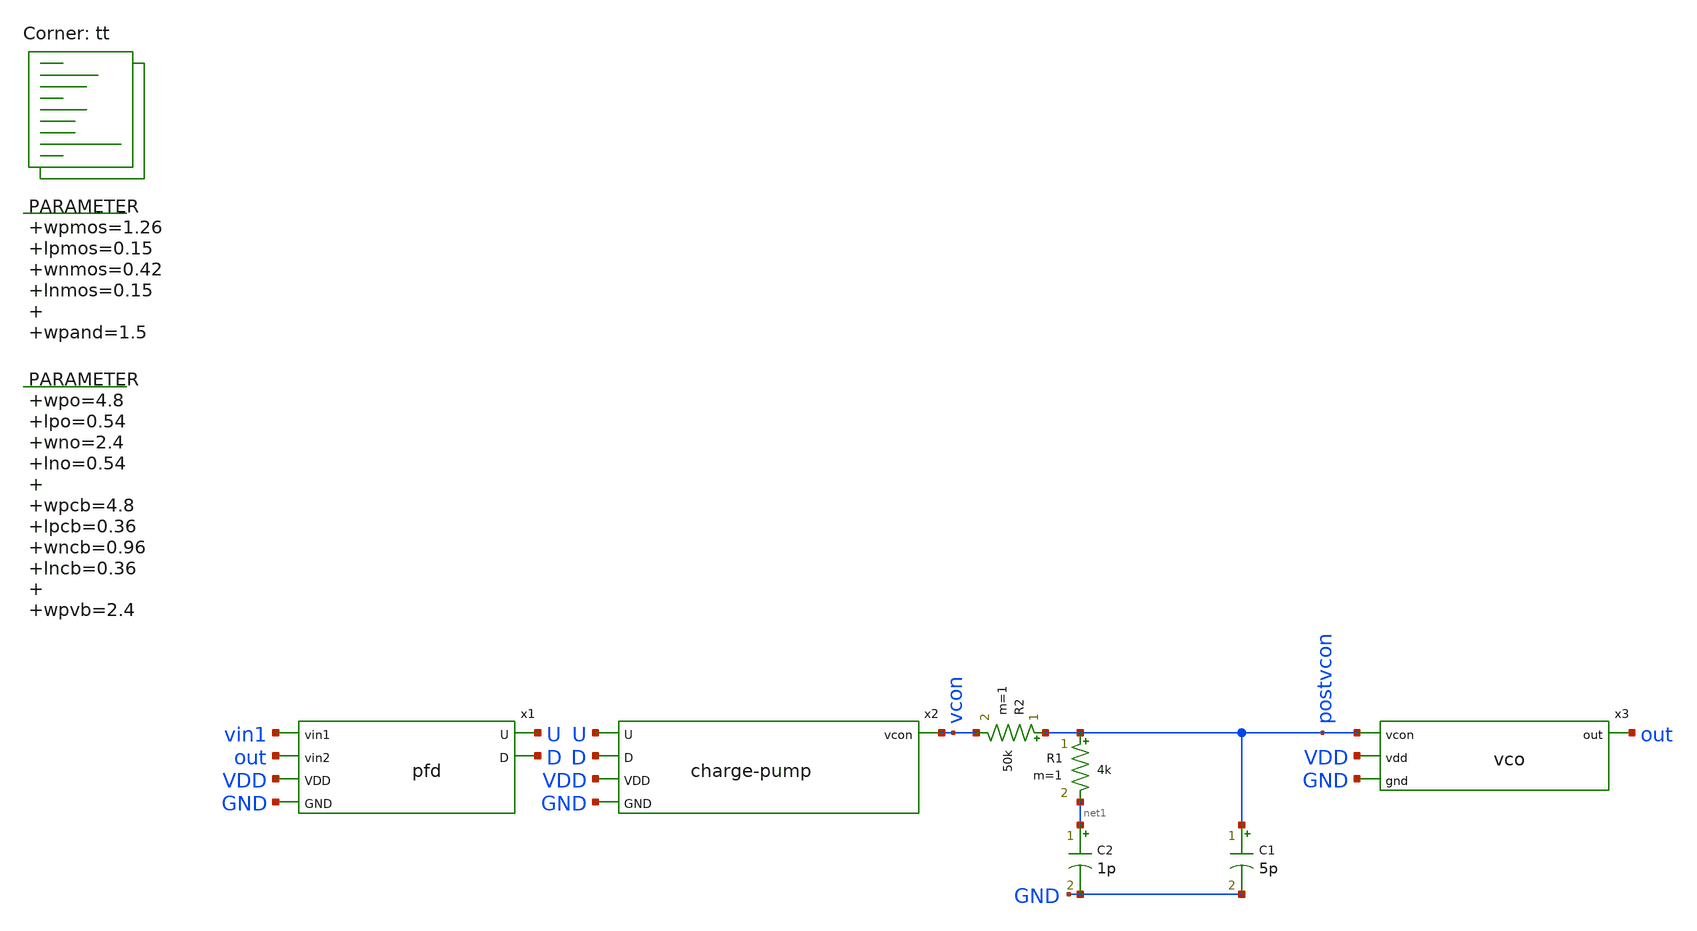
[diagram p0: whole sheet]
** sch_path: xschem/pll-tb.sch
**.subckt pll-tb
.param wpmos=1.26 lpmos=0.15 wnmos=0.42 lnmos=0.15 wpand=1.5

x2 U D vcon VDD GND charge-pump
x1 vin1 out U D VDD GND pfd
C2 net1 GND 1p m=1
R1 postvcon net1 4k m=1
R2 postvcon vcon 50k m=1
C1 postvcon GND 5p m=1
x3 postvcon out VDD GND vco
.param wpo=4.8 lpo=0.54 wno=2.4 lno=0.54 wpcb=4.8 lpcb=0.36 wncb=0.96 lncb=0.36 wpvb=2.4 lpvb=0.36
+ wnvc=96 lnvc=0.9 wpbuff=4.8 lpbuff=0.18 wnbuff=1.2 lnbuff=0.18 lres=3.5

**** begin user architecture code
 .lib $::SKYWATER_MODELS/sky130.lib.spice tt
.include $::SKYWATER_STDCELLS/sky130_fd_sc_hd.spice
.param mc_mm_switch = 0
.param mc_pr_switch = 0




  .param max_freq=100e6 period={1/max_freq} time_high={period/2}
  .param delay_vin1={time_high} delay_vin2={time_high*1.5}

  .option wnflag=1
  .option safecurrents

  *Vvdd  VDDA  VSS dc 1.8
  Vvdd1 VDD   GND dc 1.8
  Vin1 vin1 GND pulse(0 1.8 {delay_vin1} 1p 1p {time_high} {period})
  *Vin2 vin2 gnd pulse(0 1.8 {delay_vin2} 1p 1p {time_high} {period})

  .control
     reset
     save all
     tran 0.01n 1u
     write pll-tb.raw
     *set appendwrite

     *1=0 1.5=90 2=180 3=360
     *let phase=1

     *while phase <= 2
      *alter @vin2[PULSE] [ 0 1.8 {delay_vin2*$&phase} 1p 1p {time_high} {period}) ]
      *reset
      *save all
      *tran 0.01n 300n
      *write pll-tb.raw
      *let phase = phase + 0.25
     *end
    quit 0
  .endc



**** end user architecture code
**.ends

* expanding   symbol:  charge-pump.sym # of pins=5
** sym_path: xschem/charge-pump.sym
** sch_path: xschem/charge-pump.sch
.subckt charge-pump U D vcon VDD GND
*.ipin U
*.ipin D
*.opin vcon
*.ipin VDD
*.ipin GND
XM1 vcon Ub VDD VDD sky130_fd_pr__pfet_01v8 L=0.36 W=4.8 nf=1 ad='int((nf+1)/2) * W/nf * 0.29' as='int((nf+2)/2) * W/nf * 0.29'
+ pd='2*int((nf+1)/2) * (W/nf + 0.29)' ps='2*int((nf+2)/2) * (W/nf + 0.29)' nrd='0.29 / W' nrs='0.29 / W'
+ sa=0 sb=0 sd=0 mult=1 m=1
XM2 vcon D GND GND sky130_fd_pr__nfet_01v8 L=0.36 W=0.96 nf=1 ad='int((nf+1)/2) * W/nf * 0.29' as='int((nf+2)/2) * W/nf * 0.29'
+ pd='2*int((nf+1)/2) * (W/nf + 0.29)' ps='2*int((nf+2)/2) * (W/nf + 0.29)' nrd='0.29 / W' nrs='0.29 / W'
+ sa=0 sb=0 sd=0 mult=1 m=1
XM3 Ub U VDD VDD sky130_fd_pr__pfet_01v8 L=0.18 W=4.8 nf=1 ad='int((nf+1)/2) * W/nf * 0.29' as='int((nf+2)/2) * W/nf * 0.29'
+ pd='2*int((nf+1)/2) * (W/nf + 0.29)' ps='2*int((nf+2)/2) * (W/nf + 0.29)' nrd='0.29 / W' nrs='0.29 / W'
+ sa=0 sb=0 sd=0 mult=1 m=1
XM4 Ub U GND GND sky130_fd_pr__nfet_01v8 L=0.18 W=1.2 nf=1 ad='int((nf+1)/2) * W/nf * 0.29' as='int((nf+2)/2) * W/nf * 0.29'
+ pd='2*int((nf+1)/2) * (W/nf + 0.29)' ps='2*int((nf+2)/2) * (W/nf + 0.29)' nrd='0.29 / W' nrs='0.29 / W'
+ sa=0 sb=0 sd=0 mult=1 m=1
.ends


* expanding   symbol:  pfd.sym # of pins=6
** sym_path: xschem/pfd.sym
** sch_path: xschem/pfd.sch
.subckt pfd vin1 vin2 U D VDD GND
*.ipin vin1
*.ipin vin2
*.opin U
*.opin D
*.ipin VDD
*.ipin GND
.param wpmos=1.26 lpmos=0.15 wnmos=0.42 lnmos=0.15 wpand=1.5

XM1 net4 rst GND GND sky130_fd_pr__nfet_01v8 L=lnmos W=wnmos nf=1 ad='int((nf+1)/2) * W/nf * 0.29' as='int((nf+2)/2) * W/nf * 0.29'
+ pd='2*int((nf+1)/2) * (W/nf + 0.29)' ps='2*int((nf+2)/2) * (W/nf + 0.29)' nrd='0.29 / W' nrs='0.29 / W'
+ sa=0 sb=0 sd=0 mult=1 m=1
XM2 net3 vin1 VDD VDD sky130_fd_pr__pfet_01v8 L=lpmos W=wpmos nf=1 ad='int((nf+1)/2) * W/nf * 0.29' as='int((nf+2)/2) * W/nf * 0.29'
+ pd='2*int((nf+1)/2) * (W/nf + 0.29)' ps='2*int((nf+2)/2) * (W/nf + 0.29)' nrd='0.29 / W' nrs='0.29 / W'
+ sa=0 sb=0 sd=0 mult=1 m=1
XM3 net4 rst net3 VDD sky130_fd_pr__pfet_01v8 L=lpmos W=wpmos nf=1 ad='int((nf+1)/2) * W/nf * 0.29' as='int((nf+2)/2) * W/nf * 0.29'
+ pd='2*int((nf+1)/2) * (W/nf + 0.29)' ps='2*int((nf+2)/2) * (W/nf + 0.29)' nrd='0.29 / W' nrs='0.29 / W'
+ sa=0 sb=0 sd=0 mult=1 m=1
XM4 net1 net4 VDD VDD sky130_fd_pr__pfet_01v8 L=lpmos W=wpmos nf=1 ad='int((nf+1)/2) * W/nf * 0.29' as='int((nf+2)/2) * W/nf * 0.29'
+ pd='2*int((nf+1)/2) * (W/nf + 0.29)' ps='2*int((nf+2)/2) * (W/nf + 0.29)' nrd='0.29 / W' nrs='0.29 / W'
+ sa=0 sb=0 sd=0 mult=1 m=1
XM5 preU net1 VDD VDD sky130_fd_pr__pfet_01v8 L=lpmos W=wpmos nf=1 ad='int((nf+1)/2) * W/nf * 0.29' as='int((nf+2)/2) * W/nf * 0.29'
+ pd='2*int((nf+1)/2) * (W/nf + 0.29)' ps='2*int((nf+2)/2) * (W/nf + 0.29)' nrd='0.29 / W' nrs='0.29 / W'
+ sa=0 sb=0 sd=0 mult=1 m=1
XM6 net1 net4 net2 GND sky130_fd_pr__nfet_01v8 L=lnmos W=wnmos nf=1 ad='int((nf+1)/2) * W/nf * 0.29'
+ as='int((nf+2)/2) * W/nf * 0.29' pd='2*int((nf+1)/2) * (W/nf + 0.29)' ps='2*int((nf+2)/2) * (W/nf + 0.29)'
+ nrd='0.29 / W' nrs='0.29 / W' sa=0 sb=0 sd=0 mult=1 m=1
XM7 preU net1 GND GND sky130_fd_pr__nfet_01v8 L=lnmos W=wnmos nf=1 ad='int((nf+1)/2) * W/nf * 0.29' as='int((nf+2)/2) * W/nf * 0.29'
+ pd='2*int((nf+1)/2) * (W/nf + 0.29)' ps='2*int((nf+2)/2) * (W/nf + 0.29)' nrd='0.29 / W' nrs='0.29 / W'
+ sa=0 sb=0 sd=0 mult=1 m=1
XM8 net2 vin1 GND GND sky130_fd_pr__nfet_01v8 L=lnmos W=wnmos nf=1 ad='int((nf+1)/2) * W/nf * 0.29' as='int((nf+2)/2) * W/nf * 0.29'
+ pd='2*int((nf+1)/2) * (W/nf + 0.29)' ps='2*int((nf+2)/2) * (W/nf + 0.29)' nrd='0.29 / W' nrs='0.29 / W'
+ sa=0 sb=0 sd=0 mult=1 m=1
XM10 net6 vin2 VDD VDD sky130_fd_pr__pfet_01v8 L=lpmos W=wpmos nf=1 ad='int((nf+1)/2) * W/nf * 0.29'
+ as='int((nf+2)/2) * W/nf * 0.29' pd='2*int((nf+1)/2) * (W/nf + 0.29)' ps='2*int((nf+2)/2) * (W/nf + 0.29)'
+ nrd='0.29 / W' nrs='0.29 / W' sa=0 sb=0 sd=0 mult=1 m=1
XM11 net5 net7 VDD VDD sky130_fd_pr__pfet_01v8 L=lpmos W=wpmos nf=1 ad='int((nf+1)/2) * W/nf * 0.29'
+ as='int((nf+2)/2) * W/nf * 0.29' pd='2*int((nf+1)/2) * (W/nf + 0.29)' ps='2*int((nf+2)/2) * (W/nf + 0.29)'
+ nrd='0.29 / W' nrs='0.29 / W' sa=0 sb=0 sd=0 mult=1 m=1
XM12 net7 rst net6 VDD sky130_fd_pr__pfet_01v8 L=lpmos W=wpmos nf=1 ad='int((nf+1)/2) * W/nf * 0.29'
+ as='int((nf+2)/2) * W/nf * 0.29' pd='2*int((nf+1)/2) * (W/nf + 0.29)' ps='2*int((nf+2)/2) * (W/nf + 0.29)'
+ nrd='0.29 / W' nrs='0.29 / W' sa=0 sb=0 sd=0 mult=1 m=1
XM13 preD net5 VDD VDD sky130_fd_pr__pfet_01v8 L=lpmos W=wpmos nf=1 ad='int((nf+1)/2) * W/nf * 0.29'
+ as='int((nf+2)/2) * W/nf * 0.29' pd='2*int((nf+1)/2) * (W/nf + 0.29)' ps='2*int((nf+2)/2) * (W/nf + 0.29)'
+ nrd='0.29 / W' nrs='0.29 / W' sa=0 sb=0 sd=0 mult=1 m=1
XM14 net7 rst GND GND sky130_fd_pr__nfet_01v8 L=lnmos W=wnmos nf=1 ad='int((nf+1)/2) * W/nf * 0.29' as='int((nf+2)/2) * W/nf * 0.29'
+ pd='2*int((nf+1)/2) * (W/nf + 0.29)' ps='2*int((nf+2)/2) * (W/nf + 0.29)' nrd='0.29 / W' nrs='0.29 / W'
+ sa=0 sb=0 sd=0 mult=1 m=1
XM15 net5 net7 net8 GND sky130_fd_pr__nfet_01v8 L=lnmos W=wnmos nf=1 ad='int((nf+1)/2) * W/nf * 0.29'
+ as='int((nf+2)/2) * W/nf * 0.29' pd='2*int((nf+1)/2) * (W/nf + 0.29)' ps='2*int((nf+2)/2) * (W/nf + 0.29)'
+ nrd='0.29 / W' nrs='0.29 / W' sa=0 sb=0 sd=0 mult=1 m=1
XM16 preD net5 GND GND sky130_fd_pr__nfet_01v8 L=lnmos W=wnmos nf=1 ad='int((nf+1)/2) * W/nf * 0.29'
+ as='int((nf+2)/2) * W/nf * 0.29' pd='2*int((nf+1)/2) * (W/nf + 0.29)' ps='2*int((nf+2)/2) * (W/nf + 0.29)'
+ nrd='0.29 / W' nrs='0.29 / W' sa=0 sb=0 sd=0 mult=1 m=1
XM18 net8 vin2 GND GND sky130_fd_pr__nfet_01v8 L=lnmos W=wnmos nf=1 ad='int((nf+1)/2) * W/nf * 0.29'
+ as='int((nf+2)/2) * W/nf * 0.29' pd='2*int((nf+1)/2) * (W/nf + 0.29)' ps='2*int((nf+2)/2) * (W/nf + 0.29)'
+ nrd='0.29 / W' nrs='0.29 / W' sa=0 sb=0 sd=0 mult=1 m=1
x1 preU GND GND VDD VDD U sky130_fd_sc_hd__buf_8
x2 preD GND GND VDD VDD D sky130_fd_sc_hd__buf_8
x3 prerst GND GND VDD VDD rst sky130_fd_sc_hd__buf_1
x4 U D GND GND VDD VDD prerst sky130_fd_sc_hd__and2_1
.ends


* expanding   symbol:  vco.sym # of pins=4
** sym_path: xschem/vco.sym
** sch_path: xschem/vco.sch
.subckt vco vcon out vdd gnd
*.ipin vcon
*.opin out
*.ipin vdd
*.ipin gnd
.param wpo=4.8 lpo=0.54 wno=2.4 lno=0.54 wpcb=4.8 lpcb=0.36 wncb=0.96 lncb=0.36 wpvb=6 lpvb=0.9
+ wnvc=96 lnvc=0.9 wpbuff=4.8 lpbuff=0.18 wnbuff=1.2 lnbuff=0.18 lres=3.5

XM1 vnbias vnbias gnd gnd sky130_fd_pr__nfet_01v8 L=lncb W=wncb nf=1 ad='int((nf+1)/2) * W/nf * 0.29'
+ as='int((nf+2)/2) * W/nf * 0.29' pd='2*int((nf+1)/2) * (W/nf + 0.29)' ps='2*int((nf+2)/2) * (W/nf + 0.29)'
+ nrd='0.29 / W' nrs='0.29 / W' sa=0 sb=0 sd=0 mult=1 m=1
XM2 vpbias vpbias vdd vdd sky130_fd_pr__pfet_01v8 L=lpvb W=wpvb nf=1 ad='int((nf+1)/2) * W/nf * 0.29'
+ as='int((nf+2)/2) * W/nf * 0.29' pd='2*int((nf+1)/2) * (W/nf + 0.29)' ps='2*int((nf+2)/2) * (W/nf + 0.29)'
+ nrd='0.29 / W' nrs='0.29 / W' sa=0 sb=0 sd=0 mult=1 m=1
XM4 vnbias vpbias vdd vdd sky130_fd_pr__pfet_01v8 L=lpcb W=wpcb nf=1 ad='int((nf+1)/2) * W/nf * 0.29'
+ as='int((nf+2)/2) * W/nf * 0.29' pd='2*int((nf+1)/2) * (W/nf + 0.29)' ps='2*int((nf+2)/2) * (W/nf + 0.29)'
+ nrd='0.29 / W' nrs='0.29 / W' sa=0 sb=0 sd=0 mult=1 m=1
XM5 net8 net9 net1 gnd sky130_fd_pr__nfet_01v8 L=lno W=wno nf=1 ad='int((nf+1)/2) * W/nf * 0.29' as='int((nf+2)/2) * W/nf * 0.29'
+ pd='2*int((nf+1)/2) * (W/nf + 0.29)' ps='2*int((nf+2)/2) * (W/nf + 0.29)' nrd='0.29 / W' nrs='0.29 / W'
+ sa=0 sb=0 sd=0 mult=1 m=1
XM6 net8 net9 net12 vdd sky130_fd_pr__pfet_01v8 L=lpo W=wpo nf=1 ad='int((nf+1)/2) * W/nf * 0.29' as='int((nf+2)/2) * W/nf * 0.29'
+ pd='2*int((nf+1)/2) * (W/nf + 0.29)' ps='2*int((nf+2)/2) * (W/nf + 0.29)' nrd='0.29 / W' nrs='0.29 / W'
+ sa=0 sb=0 sd=0 mult=1 m=1
XM7 net7 net8 net2 gnd sky130_fd_pr__nfet_01v8 L=lno W=wno nf=1 ad='int((nf+1)/2) * W/nf * 0.29' as='int((nf+2)/2) * W/nf * 0.29'
+ pd='2*int((nf+1)/2) * (W/nf + 0.29)' ps='2*int((nf+2)/2) * (W/nf + 0.29)' nrd='0.29 / W' nrs='0.29 / W'
+ sa=0 sb=0 sd=0 mult=1 m=1
XM8 net7 net8 net13 vdd sky130_fd_pr__pfet_01v8 L=lpo W=wpo nf=1 ad='int((nf+1)/2) * W/nf * 0.29' as='int((nf+2)/2) * W/nf * 0.29'
+ pd='2*int((nf+1)/2) * (W/nf + 0.29)' ps='2*int((nf+2)/2) * (W/nf + 0.29)' nrd='0.29 / W' nrs='0.29 / W'
+ sa=0 sb=0 sd=0 mult=1 m=1
XM9 net6 net7 net3 gnd sky130_fd_pr__nfet_01v8 L=lno W=wno nf=1 ad='int((nf+1)/2) * W/nf * 0.29' as='int((nf+2)/2) * W/nf * 0.29'
+ pd='2*int((nf+1)/2) * (W/nf + 0.29)' ps='2*int((nf+2)/2) * (W/nf + 0.29)' nrd='0.29 / W' nrs='0.29 / W'
+ sa=0 sb=0 sd=0 mult=1 m=1
XM10 net6 net7 net14 vdd sky130_fd_pr__pfet_01v8 L=lpo W=wpo nf=1 ad='int((nf+1)/2) * W/nf * 0.29' as='int((nf+2)/2) * W/nf * 0.29'
+ pd='2*int((nf+1)/2) * (W/nf + 0.29)' ps='2*int((nf+2)/2) * (W/nf + 0.29)' nrd='0.29 / W' nrs='0.29 / W'
+ sa=0 sb=0 sd=0 mult=1 m=1
XM11 net10 net6 net5 gnd sky130_fd_pr__nfet_01v8 L=lno W=wno nf=1 ad='int((nf+1)/2) * W/nf * 0.29' as='int((nf+2)/2) * W/nf * 0.29'
+ pd='2*int((nf+1)/2) * (W/nf + 0.29)' ps='2*int((nf+2)/2) * (W/nf + 0.29)' nrd='0.29 / W' nrs='0.29 / W'
+ sa=0 sb=0 sd=0 mult=1 m=1
XM12 net10 net6 net15 vdd sky130_fd_pr__pfet_01v8 L=lpo W=wpo nf=1 ad='int((nf+1)/2) * W/nf * 0.29' as='int((nf+2)/2) * W/nf * 0.29'
+ pd='2*int((nf+1)/2) * (W/nf + 0.29)' ps='2*int((nf+2)/2) * (W/nf + 0.29)' nrd='0.29 / W' nrs='0.29 / W'
+ sa=0 sb=0 sd=0 mult=1 m=1
XM13 net9 net10 net4 gnd sky130_fd_pr__nfet_01v8 L=lno W=wno nf=1 ad='int((nf+1)/2) * W/nf * 0.29' as='int((nf+2)/2) * W/nf * 0.29'
+ pd='2*int((nf+1)/2) * (W/nf + 0.29)' ps='2*int((nf+2)/2) * (W/nf + 0.29)' nrd='0.29 / W' nrs='0.29 / W'
+ sa=0 sb=0 sd=0 mult=1 m=1
XM14 net9 net10 net16 vdd sky130_fd_pr__pfet_01v8 L=lpo W=wpo nf=1 ad='int((nf+1)/2) * W/nf * 0.29' as='int((nf+2)/2) * W/nf * 0.29'
+ pd='2*int((nf+1)/2) * (W/nf + 0.29)' ps='2*int((nf+2)/2) * (W/nf + 0.29)' nrd='0.29 / W' nrs='0.29 / W'
+ sa=0 sb=0 sd=0 mult=1 m=1
XM16 net12 vpbias vdd vdd sky130_fd_pr__pfet_01v8 L=lpcb W=wpcb nf=1 ad='int((nf+1)/2) * W/nf * 0.29'
+ as='int((nf+2)/2) * W/nf * 0.29' pd='2*int((nf+1)/2) * (W/nf + 0.29)' ps='2*int((nf+2)/2) * (W/nf + 0.29)'
+ nrd='0.29 / W' nrs='0.29 / W' sa=0 sb=0 sd=0 mult=1 m=1
XM18 net13 vpbias vdd vdd sky130_fd_pr__pfet_01v8 L=lpcb W=wpcb nf=1 ad='int((nf+1)/2) * W/nf * 0.29'
+ as='int((nf+2)/2) * W/nf * 0.29' pd='2*int((nf+1)/2) * (W/nf + 0.29)' ps='2*int((nf+2)/2) * (W/nf + 0.29)'
+ nrd='0.29 / W' nrs='0.29 / W' sa=0 sb=0 sd=0 mult=1 m=1
XM20 net14 vpbias vdd vdd sky130_fd_pr__pfet_01v8 L=lpcb W=wpcb nf=1 ad='int((nf+1)/2) * W/nf * 0.29'
+ as='int((nf+2)/2) * W/nf * 0.29' pd='2*int((nf+1)/2) * (W/nf + 0.29)' ps='2*int((nf+2)/2) * (W/nf + 0.29)'
+ nrd='0.29 / W' nrs='0.29 / W' sa=0 sb=0 sd=0 mult=1 m=1
XM22 net15 vpbias vdd vdd sky130_fd_pr__pfet_01v8 L=lpcb W=wpcb nf=1 ad='int((nf+1)/2) * W/nf * 0.29'
+ as='int((nf+2)/2) * W/nf * 0.29' pd='2*int((nf+1)/2) * (W/nf + 0.29)' ps='2*int((nf+2)/2) * (W/nf + 0.29)'
+ nrd='0.29 / W' nrs='0.29 / W' sa=0 sb=0 sd=0 mult=1 m=1
XM24 net16 vpbias vdd vdd sky130_fd_pr__pfet_01v8 L=lpcb W=wpcb nf=1 ad='int((nf+1)/2) * W/nf * 0.29'
+ as='int((nf+2)/2) * W/nf * 0.29' pd='2*int((nf+1)/2) * (W/nf + 0.29)' ps='2*int((nf+2)/2) * (W/nf + 0.29)'
+ nrd='0.29 / W' nrs='0.29 / W' sa=0 sb=0 sd=0 mult=1 m=1
XM25 net11 net9 gnd gnd sky130_fd_pr__nfet_01v8 L=lnbuff W=wnbuff nf=1 ad='int((nf+1)/2) * W/nf * 0.29'
+ as='int((nf+2)/2) * W/nf * 0.29' pd='2*int((nf+1)/2) * (W/nf + 0.29)' ps='2*int((nf+2)/2) * (W/nf + 0.29)'
+ nrd='0.29 / W' nrs='0.29 / W' sa=0 sb=0 sd=0 mult=1 m=1
XM26 net11 net9 vdd vdd sky130_fd_pr__pfet_01v8 L=lpbuff W=wpbuff nf=1 ad='int((nf+1)/2) * W/nf * 0.29'
+ as='int((nf+2)/2) * W/nf * 0.29' pd='2*int((nf+1)/2) * (W/nf + 0.29)' ps='2*int((nf+2)/2) * (W/nf + 0.29)'
+ nrd='0.29 / W' nrs='0.29 / W' sa=0 sb=0 sd=0 mult=1 m=1
XM27 out net11 gnd gnd sky130_fd_pr__nfet_01v8 L=lnbuff W=wnbuff nf=1 ad='int((nf+1)/2) * W/nf * 0.29'
+ as='int((nf+2)/2) * W/nf * 0.29' pd='2*int((nf+1)/2) * (W/nf + 0.29)' ps='2*int((nf+2)/2) * (W/nf + 0.29)'
+ nrd='0.29 / W' nrs='0.29 / W' sa=0 sb=0 sd=0 mult=1 m=1
XM28 out net11 vdd vdd sky130_fd_pr__pfet_01v8 L=lpbuff W=wpbuff nf=1 ad='int((nf+1)/2) * W/nf * 0.29'
+ as='int((nf+2)/2) * W/nf * 0.29' pd='2*int((nf+1)/2) * (W/nf + 0.29)' ps='2*int((nf+2)/2) * (W/nf + 0.29)'
+ nrd='0.29 / W' nrs='0.29 / W' sa=0 sb=0 sd=0 mult=1 m=1
XM15 net1 vnbias gnd gnd sky130_fd_pr__nfet_01v8 L=lncb W=wncb nf=1 ad='int((nf+1)/2) * W/nf * 0.29'
+ as='int((nf+2)/2) * W/nf * 0.29' pd='2*int((nf+1)/2) * (W/nf + 0.29)' ps='2*int((nf+2)/2) * (W/nf + 0.29)'
+ nrd='0.29 / W' nrs='0.29 / W' sa=0 sb=0 sd=0 mult=1 m=1
XM17 net2 vnbias gnd gnd sky130_fd_pr__nfet_01v8 L=lncb W=wncb nf=1 ad='int((nf+1)/2) * W/nf * 0.29'
+ as='int((nf+2)/2) * W/nf * 0.29' pd='2*int((nf+1)/2) * (W/nf + 0.29)' ps='2*int((nf+2)/2) * (W/nf + 0.29)'
+ nrd='0.29 / W' nrs='0.29 / W' sa=0 sb=0 sd=0 mult=1 m=1
XM19 net3 vnbias gnd gnd sky130_fd_pr__nfet_01v8 L=lncb W=wncb nf=1 ad='int((nf+1)/2) * W/nf * 0.29'
+ as='int((nf+2)/2) * W/nf * 0.29' pd='2*int((nf+1)/2) * (W/nf + 0.29)' ps='2*int((nf+2)/2) * (W/nf + 0.29)'
+ nrd='0.29 / W' nrs='0.29 / W' sa=0 sb=0 sd=0 mult=1 m=1
XM21 net5 vnbias gnd gnd sky130_fd_pr__nfet_01v8 L=lncb W=wncb nf=1 ad='int((nf+1)/2) * W/nf * 0.29'
+ as='int((nf+2)/2) * W/nf * 0.29' pd='2*int((nf+1)/2) * (W/nf + 0.29)' ps='2*int((nf+2)/2) * (W/nf + 0.29)'
+ nrd='0.29 / W' nrs='0.29 / W' sa=0 sb=0 sd=0 mult=1 m=1
XM23 net4 vnbias gnd gnd sky130_fd_pr__nfet_01v8 L=lncb W=wncb nf=1 ad='int((nf+1)/2) * W/nf * 0.29'
+ as='int((nf+2)/2) * W/nf * 0.29' pd='2*int((nf+1)/2) * (W/nf + 0.29)' ps='2*int((nf+2)/2) * (W/nf + 0.29)'
+ nrd='0.29 / W' nrs='0.29 / W' sa=0 sb=0 sd=0 mult=1 m=1
XR3 gnd net17 gnd sky130_fd_pr__res_xhigh_po W=0.35 L=lres mult=1 m=1
XM29 vpbias vcon net17 gnd sky130_fd_pr__nfet_01v8 L=lnvc W=wnvc nf=1 ad='int((nf+1)/2) * W/nf * 0.29'
+ as='int((nf+2)/2) * W/nf * 0.29' pd='2*int((nf+1)/2) * (W/nf + 0.29)' ps='2*int((nf+2)/2) * (W/nf + 0.29)'
+ nrd='0.29 / W' nrs='0.29 / W' sa=0 sb=0 sd=0 mult=1 m=1
.ends

.end
